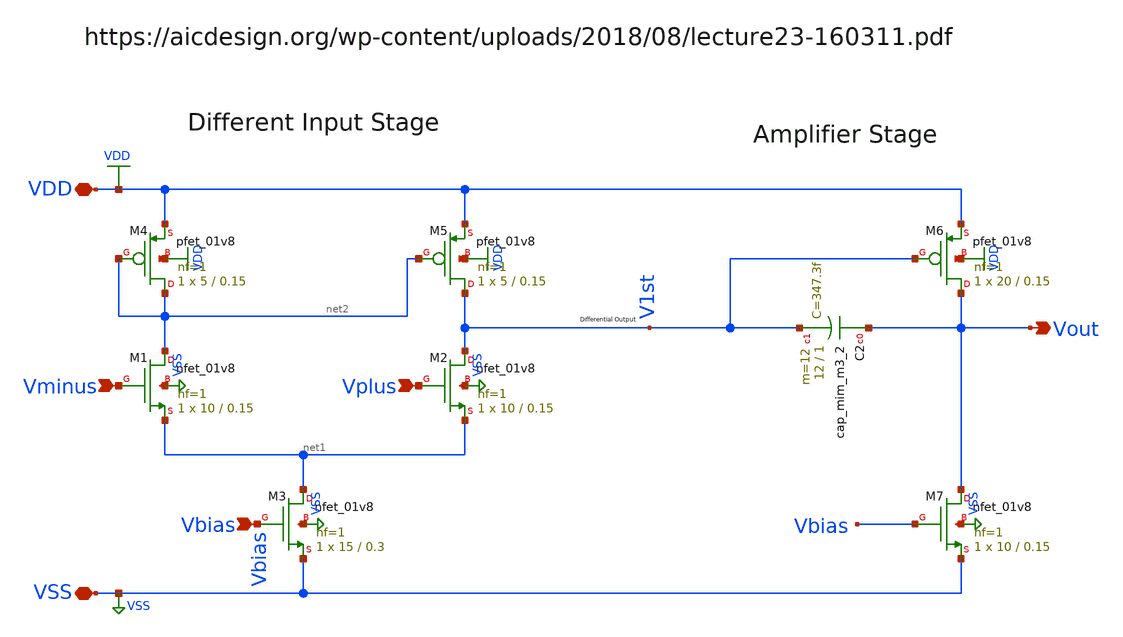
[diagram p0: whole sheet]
** sch_path: analog/library/Operational_Amplifiers/OpAmp.sch
**.subckt OpAmp Vbias Vplus Vminus Vout VDD VSS
*.ipin Vbias
*.ipin Vplus
*.ipin Vminus
*.opin Vout
*.iopin VDD
*.iopin VSS
XM1 net2 Vminus net1 VSS sky130_fd_pr__nfet_01v8 L=0.15 W=10 nf=1 ad='int((nf+1)/2) * W/nf * 0.29' as='int((nf+2)/2) * W/nf * 0.29'
+ pd='2*int((nf+1)/2) * (W/nf + 0.29)' ps='2*int((nf+2)/2) * (W/nf + 0.29)' nrd='0.29 / W' nrs='0.29 / W'
+ sa=0 sb=0 sd=0 mult=1 m=1
XM2 V1st Vplus net1 VSS sky130_fd_pr__nfet_01v8 L=0.15 W=10 nf=1 ad='int((nf+1)/2) * W/nf * 0.29' as='int((nf+2)/2) * W/nf * 0.29'
+ pd='2*int((nf+1)/2) * (W/nf + 0.29)' ps='2*int((nf+2)/2) * (W/nf + 0.29)' nrd='0.29 / W' nrs='0.29 / W'
+ sa=0 sb=0 sd=0 mult=1 m=1
XM3 net1 Vbias VSS VSS sky130_fd_pr__nfet_01v8 L=0.3 W=15 nf=1 ad='int((nf+1)/2) * W/nf * 0.29' as='int((nf+2)/2) * W/nf * 0.29'
+ pd='2*int((nf+1)/2) * (W/nf + 0.29)' ps='2*int((nf+2)/2) * (W/nf + 0.29)' nrd='0.29 / W' nrs='0.29 / W'
+ sa=0 sb=0 sd=0 mult=1 m=1
XM4 net2 net2 VDD VDD sky130_fd_pr__pfet_01v8 L=0.15 W=5 nf=1 ad='int((nf+1)/2) * W/nf * 0.29' as='int((nf+2)/2) * W/nf * 0.29'
+ pd='2*int((nf+1)/2) * (W/nf + 0.29)' ps='2*int((nf+2)/2) * (W/nf + 0.29)' nrd='0.29 / W' nrs='0.29 / W'
+ sa=0 sb=0 sd=0 mult=1 m=1
XM5 V1st net2 VDD VDD sky130_fd_pr__pfet_01v8 L=0.15 W=5 nf=1 ad='int((nf+1)/2) * W/nf * 0.29' as='int((nf+2)/2) * W/nf * 0.29'
+ pd='2*int((nf+1)/2) * (W/nf + 0.29)' ps='2*int((nf+2)/2) * (W/nf + 0.29)' nrd='0.29 / W' nrs='0.29 / W'
+ sa=0 sb=0 sd=0 mult=1 m=1
XM6 Vout V1st VDD VDD sky130_fd_pr__pfet_01v8 L=0.15 W=20 nf=1 ad='int((nf+1)/2) * W/nf * 0.29' as='int((nf+2)/2) * W/nf * 0.29'
+ pd='2*int((nf+1)/2) * (W/nf + 0.29)' ps='2*int((nf+2)/2) * (W/nf + 0.29)' nrd='0.29 / W' nrs='0.29 / W'
+ sa=0 sb=0 sd=0 mult=1 m=1
XM7 Vout Vbias VSS VSS sky130_fd_pr__nfet_01v8 L=0.15 W=10 nf=1 ad='int((nf+1)/2) * W/nf * 0.29' as='int((nf+2)/2) * W/nf * 0.29'
+ pd='2*int((nf+1)/2) * (W/nf + 0.29)' ps='2*int((nf+2)/2) * (W/nf + 0.29)' nrd='0.29 / W' nrs='0.29 / W'
+ sa=0 sb=0 sd=0 mult=1 m=1
XC2 Vout V1st sky130_fd_pr__cap_mim_m3_2 W=12 L=1 MF=12 m=12
**.ends
.GLOBAL VSS
.GLOBAL VDD
.end
